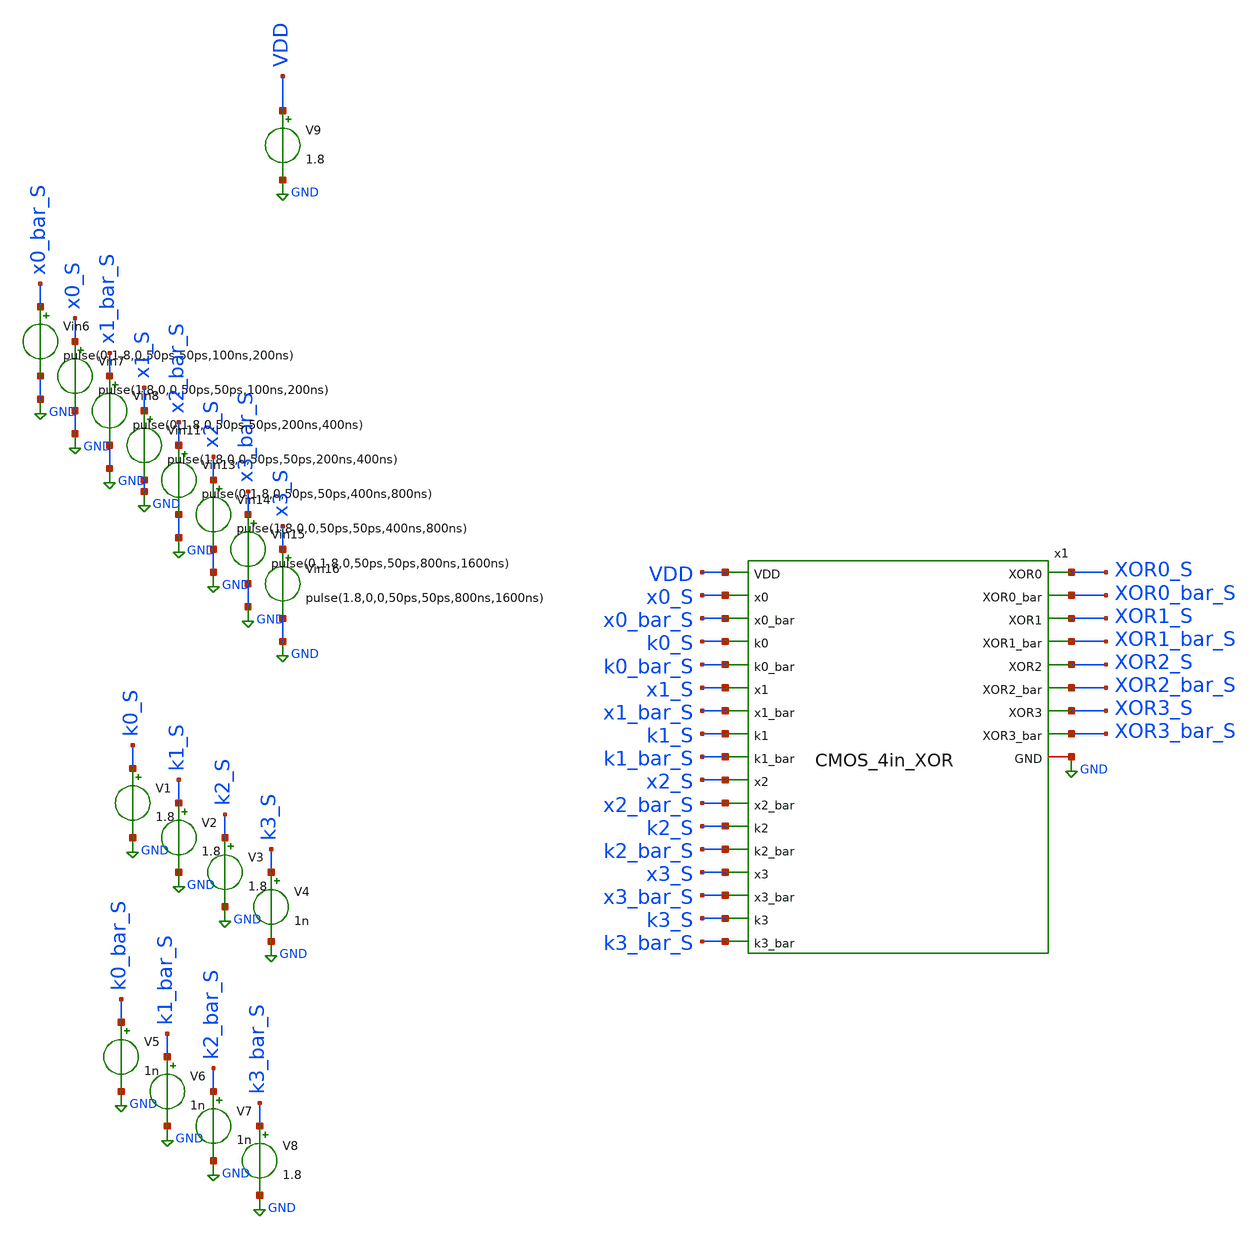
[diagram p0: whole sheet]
** sch_path: skywater_stuff/CMOS_4in_XOR_sim.sch
**.subckt CMOS_4in_XOR_sim
x1 VDD XOR0_S x0_S XOR0_bar_S x0_bar_S k0_S k0_bar_S XOR1_S x1_S XOR1_bar_S x1_bar_S k1_S k1_bar_S
+ XOR2_S x2_S x2_bar_S XOR2_bar_S k2_S k2_bar_S XOR3_S x3_S GND XOR3_bar_S x3_bar_S k3_S k3_bar_S
+ CMOS_4in_XOR
V1 k0_S GND 1.8
V2 k1_S GND 1.8
V3 k2_S GND 1.8
V4 k3_S GND 1n
V5 k0_bar_S GND 1n
V6 k1_bar_S GND 1n
V7 k2_bar_S GND 1n
V8 k3_bar_S GND 1.8
Vin6 x0_bar_S GND pulse(0,1.8,0,50ps,50ps,100ns,200ns)
Vin7 x0_S GND pulse(1.8,0,0,50ps,50ps,100ns,200ns)
Vin8 x1_bar_S GND pulse(0,1.8,0,50ps,50ps,200ns,400ns)
Vin11 x1_S GND pulse(1.8,0,0,50ps,50ps,200ns,400ns)
Vin13 x2_bar_S GND pulse(0,1.8,0,50ps,50ps,400ns,800ns)
Vin14 x2_S GND pulse(1.8,0,0,50ps,50ps,400ns,800ns)
Vin15 x3_bar_S GND pulse(0,1.8,0,50ps,50ps,800ns,1600ns)
Vin16 x3_S GND pulse(1.8,0,0,50ps,50ps,800ns,1600ns)
V9 VDD GND 1.8
**** begin user architecture code

.lib /research/pdk/open_pdks/share/pdk/sky130A/libs.tech/ngspice/sky130.lib.spice tt
**.include ~/magic_layout_stuff/EESPFAL_4in_XOR.spice
**.include ~/magic_layout_stuff/EESPFAL_4in_XOR_flat.spice
.control
save all
tran 0.1n 10u
plot v(CLK0_S) v(Dis0_S)
plot v(XOR0_S)
**plot v(XOR0_flat)
plot v(XOR1_S)
**plot v(XOR1_flat)
plot v(XOR2_S)
**plot v(XOR2_flat)
plot v(XOR3_S)
**plot v(XOR3_flat)
**let Pinst_CLK0 = (v(CLK0)*i(vclk0))
**let Pinst_CLK0_CLK2 = (v(CLK0)*i(vclk0))+(v(CLK1)*i(vclk1))+(v(CLK2)*i(vclk2))
**let Pinst_CLK0_CLK2_Dis0_Dis2 =
*+ (v(CLK0)*i(vclk0))+(v(Dis0)*i(Vdis0))+(v(CLK1)*i(vclk1))+(v(Dis1)*i(Vdis1))+(v(CLK2)*i(vclk2))+(v(Dis2)*i(Vdis2))
**plot Pinst_CLK0
**plot Pinst_CLK0_CLK2
**plot Pinst_CLK0_CLK2_Dis0_Dis2
**wrdata EESPFAL_s0_sim.raw v(s0_normal) v(s0_bar_normal)
**wrdata EESPFAL_s0_sim_PEX.raw v(s0_flat) v(s0_bar_flat)
**wrdata EESPFAL_4in_XOR_normVSPEX.csv v(XOR0_S) v(XOR0_flat) v(XOR1_S) v(XOR1_flat) v(XOR2_S)
*+ v(XOR2_flat) v(XOR3_S) v(XOR3_flat)
**wrdata s0_sim_Pinst_CLK0_CLK2.csv Pinst_CLK0_CLK2
**wrdata s0_sim_Pinst_test.csv Pinst_CLK0_CLK2 Pinst_CLK0_CLK2_Dis0_Dis2
.endc


**** end user architecture code
**.ends

* expanding   symbol:  CMOS_4in_XOR.sym # of pins=26
** sym_path: skywater_stuff/CMOS_4in_XOR.sym
** sch_path: skywater_stuff/CMOS_4in_XOR.sch
.subckt CMOS_4in_XOR VDD XOR0 x0 XOR0_bar x0_bar k0 k0_bar XOR1 x1 XOR1_bar x1_bar k1 k1_bar XOR2 x2
+ x2_bar XOR2_bar k2 k2_bar XOR3 x3 GND XOR3_bar x3_bar k3 k3_bar
*.ipin x0
*.ipin x0_bar
*.ipin x1
*.ipin x1_bar
*.ipin x2
*.ipin x2_bar
*.ipin x3
*.ipin x3_bar
*.ipin VDD
*.iopin GND
*.opin XOR0
*.opin XOR1
*.opin XOR2
*.opin XOR3
*.ipin k0
*.ipin k0_bar
*.ipin k1
*.ipin k1_bar
*.ipin k2
*.ipin k2_bar
*.ipin k3
*.ipin k3_bar
*.opin XOR0_bar
*.opin XOR1_bar
*.opin XOR2_bar
*.opin XOR3_bar
x1 x0 x0_bar k0 k0_bar XOR0 GND VDD CMOS_XOR
x2 x1 x1_bar k1 k1_bar XOR1 GND VDD CMOS_XOR
x3 x2 x2_bar k2 k2_bar XOR2 GND VDD CMOS_XOR
x4 x3 x3_bar k3 k3_bar XOR3 GND VDD CMOS_XOR
x5 VDD XOR0 XOR0_bar GND CMOS_INV
x6 VDD XOR1 XOR1_bar GND CMOS_INV
x7 VDD XOR2 XOR2_bar GND CMOS_INV
x8 VDD XOR3 XOR3_bar GND CMOS_INV
.ends


* expanding   symbol:  CMOS_XOR.sym # of pins=7
** sym_path: skywater_stuff/CMOS_XOR.sym
** sch_path: skywater_stuff/CMOS_XOR.sch
.subckt CMOS_XOR A A_bar B B_bar XOR GND VDD
*.ipin A
*.ipin A_bar
*.ipin B
*.ipin B_bar
*.opin XOR
*.iopin GND
*.ipin VDD
XM8 net4 A_bar GND GND sky130_fd_pr__nfet_01v8 L=0.15 W=1.5 nf=1 ad='int((nf+1)/2) * W/nf * 0.29' as='int((nf+2)/2) * W/nf * 0.29'
+ pd='2*int((nf+1)/2) * (W/nf + 0.29)' ps='2*int((nf+2)/2) * (W/nf + 0.29)' nrd='0.29 / W' nrs='0.29 / W'
+ sa=0 sb=0 sd=0 mult=1 m=1
XM1 XOR B net3 GND sky130_fd_pr__nfet_01v8 L=0.15 W=1.5 nf=1 ad='int((nf+1)/2) * W/nf * 0.29' as='int((nf+2)/2) * W/nf * 0.29'
+ pd='2*int((nf+1)/2) * (W/nf + 0.29)' ps='2*int((nf+2)/2) * (W/nf + 0.29)' nrd='0.29 / W' nrs='0.29 / W'
+ sa=0 sb=0 sd=0 mult=1 m=1
XM3 XOR A net1 VDD sky130_fd_pr__pfet_01v8 L=0.15 W=3 nf=1 ad='int((nf+1)/2) * W/nf * 0.29' as='int((nf+2)/2) * W/nf * 0.29'
+ pd='2*int((nf+1)/2) * (W/nf + 0.29)' ps='2*int((nf+2)/2) * (W/nf + 0.29)' nrd='0.29 / W' nrs='0.29 / W'
+ sa=0 sb=0 sd=0 mult=1 m=1
XM4 net2 B VDD VDD sky130_fd_pr__pfet_01v8 L=0.15 W=3 nf=1 ad='int((nf+1)/2) * W/nf * 0.29' as='int((nf+2)/2) * W/nf * 0.29'
+ pd='2*int((nf+1)/2) * (W/nf + 0.29)' ps='2*int((nf+2)/2) * (W/nf + 0.29)' nrd='0.29 / W' nrs='0.29 / W'
+ sa=0 sb=0 sd=0 mult=1 m=1
XM9 net1 B_bar VDD VDD sky130_fd_pr__pfet_01v8 L=0.15 W=3 nf=1 ad='int((nf+1)/2) * W/nf * 0.29' as='int((nf+2)/2) * W/nf * 0.29'
+ pd='2*int((nf+1)/2) * (W/nf + 0.29)' ps='2*int((nf+2)/2) * (W/nf + 0.29)' nrd='0.29 / W' nrs='0.29 / W'
+ sa=0 sb=0 sd=0 mult=1 m=1
XM2 XOR B_bar net4 GND sky130_fd_pr__nfet_01v8 L=0.15 W=1.5 nf=1 ad='int((nf+1)/2) * W/nf * 0.29' as='int((nf+2)/2) * W/nf * 0.29'
+ pd='2*int((nf+1)/2) * (W/nf + 0.29)' ps='2*int((nf+2)/2) * (W/nf + 0.29)' nrd='0.29 / W' nrs='0.29 / W'
+ sa=0 sb=0 sd=0 mult=1 m=1
XM5 net3 A GND GND sky130_fd_pr__nfet_01v8 L=0.15 W=1.5 nf=1 ad='int((nf+1)/2) * W/nf * 0.29' as='int((nf+2)/2) * W/nf * 0.29'
+ pd='2*int((nf+1)/2) * (W/nf + 0.29)' ps='2*int((nf+2)/2) * (W/nf + 0.29)' nrd='0.29 / W' nrs='0.29 / W'
+ sa=0 sb=0 sd=0 mult=1 m=1
XM10 XOR A_bar net2 VDD sky130_fd_pr__pfet_01v8 L=0.15 W=3 nf=1 ad='int((nf+1)/2) * W/nf * 0.29' as='int((nf+2)/2) * W/nf * 0.29'
+ pd='2*int((nf+1)/2) * (W/nf + 0.29)' ps='2*int((nf+2)/2) * (W/nf + 0.29)' nrd='0.29 / W' nrs='0.29 / W'
+ sa=0 sb=0 sd=0 mult=1 m=1
.ends


* expanding   symbol:  CMOS_INV.sym # of pins=4
** sym_path: skywater_stuff/CMOS_INV.sym
** sch_path: skywater_stuff/CMOS_INV.sch
.subckt CMOS_INV VDD A OUT GND
*.iopin GND
*.ipin A
*.ipin VDD
*.opin OUT
XM1 OUT A VDD VDD sky130_fd_pr__pfet_01v8 L=0.15 W=3 nf=1 ad='int((nf+1)/2) * W/nf * 0.29' as='int((nf+2)/2) * W/nf * 0.29'
+ pd='2*int((nf+1)/2) * (W/nf + 0.29)' ps='2*int((nf+2)/2) * (W/nf + 0.29)' nrd='0.29 / W' nrs='0.29 / W'
+ sa=0 sb=0 sd=0 mult=1 m=1
XM2 OUT A GND GND sky130_fd_pr__nfet_01v8 L=0.15 W=1.5 nf=1 ad='int((nf+1)/2) * W/nf * 0.29' as='int((nf+2)/2) * W/nf * 0.29'
+ pd='2*int((nf+1)/2) * (W/nf + 0.29)' ps='2*int((nf+2)/2) * (W/nf + 0.29)' nrd='0.29 / W' nrs='0.29 / W'
+ sa=0 sb=0 sd=0 mult=1 m=1
.ends

.GLOBAL GND
.end
